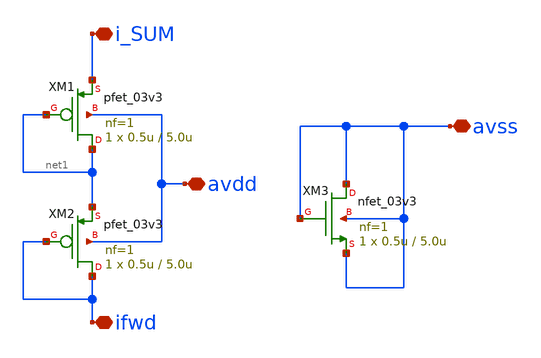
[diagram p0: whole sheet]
** sch_path: designs/libs/snn_analog/sch/Current_limit/Current-limit.sch
**.subckt Current-limit avdd avss i_SUM ifwd
*.iopin avdd
*.iopin avss
*.iopin i_SUM
*.iopin ifwd
XM1 net1 net1 i_SUM avdd pfet_03v3 L=5.0u W=0.5u nf=1 ad='int((nf+1)/2) * W/nf * 0.18u' as='int((nf+2)/2) * W/nf * 0.18u'
+ pd='2*int((nf+1)/2) * (W/nf + 0.18u)' ps='2*int((nf+2)/2) * (W/nf + 0.18u)' nrd='0.18u / W' nrs='0.18u / W'
+ sa=0 sb=0 sd=0 m=1
XM2 ifwd ifwd net1 avdd pfet_03v3 L=5.0u W=0.5u nf=1 ad='int((nf+1)/2) * W/nf * 0.18u' as='int((nf+2)/2) * W/nf * 0.18u'
+ pd='2*int((nf+1)/2) * (W/nf + 0.18u)' ps='2*int((nf+2)/2) * (W/nf + 0.18u)' nrd='0.18u / W' nrs='0.18u / W'
+ sa=0 sb=0 sd=0 m=1
XM3 avss avss avss avss nfet_03v3 L=5.0u W=0.5u nf=1 ad='int((nf+1)/2) * W/nf * 0.18u' as='int((nf+2)/2) * W/nf * 0.18u'
+ pd='2*int((nf+1)/2) * (W/nf + 0.18u)' ps='2*int((nf+2)/2) * (W/nf + 0.18u)' nrd='0.18u / W' nrs='0.18u / W'
+ sa=0 sb=0 sd=0 m=1
**.ends
.end
